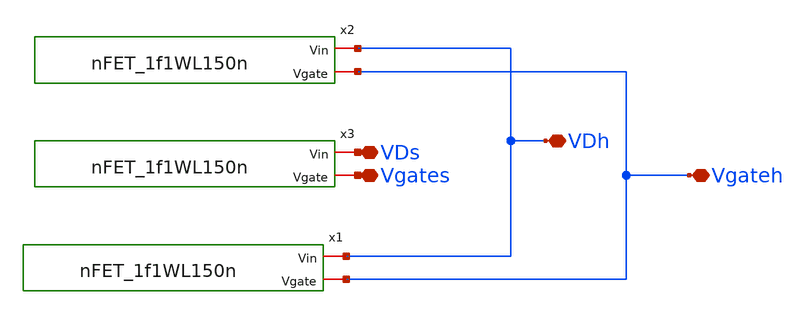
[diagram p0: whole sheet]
** sch_path: xschem/HSense_nFET_1f1WL150n_V2.sch
**.subckt HSense_nFET_1f1WL150n_V2 Vgateh VDh VDs Vgates
*.iopin Vgateh
*.iopin VDh
*.iopin VDs
*.iopin Vgates
x1 VDh Vgateh nFET_1f1WL150n
x2 VDh Vgateh nFET_1f1WL150n
x3 VDs Vgates nFET_1f1WL150n
**.ends

* expanding   symbol:  nFET_1f1WL150n.sym # of pins=2
** sym_path: xschem/nFET_1f1WL150n.sym
** sch_path: xschem/nFET_1f1WL150n.sch
.subckt nFET_1f1WL150n Vin Vgate
*.iopin Vgate
*.iopin Vin
XM1 Vin Vgate GND GND sky130_fd_pr__nfet_01v8 L=0.15 W=1 nf=1 ad='int((nf+1)/2) * W/nf * 0.29' as='int((nf+2)/2) * W/nf * 0.29'
+ pd='2*int((nf+1)/2) * (W/nf + 0.29)' ps='2*int((nf+2)/2) * (W/nf + 0.29)' nrd='0.29 / W' nrs='0.29 / W'
+ sa=0 sb=0 sd=0 mult=1 m=1
.ends

.GLOBAL GND
.end
